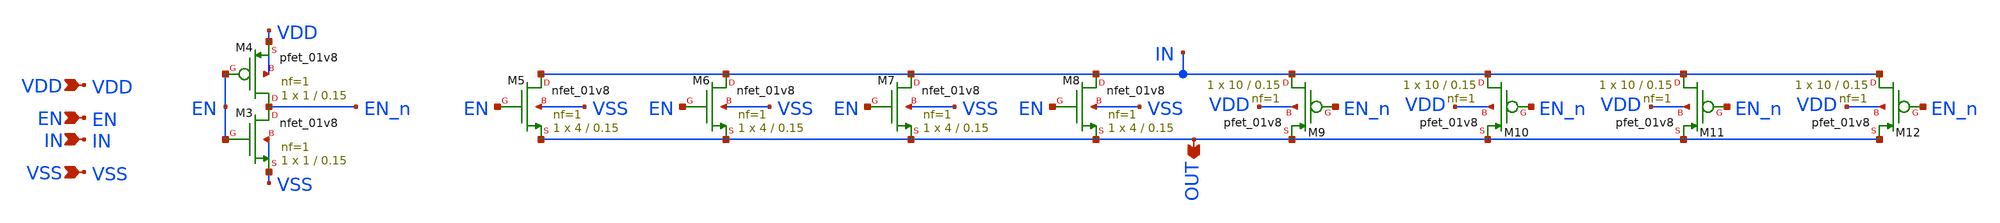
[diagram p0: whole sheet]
** sch_path: xschem/anl_switch.sch
**.subckt anl_switch IN VDD VSS EN OUT
*.ipin IN
*.ipin VDD
*.ipin VSS
*.ipin EN
*.opin OUT
XM3 EN_n EN VSS VSS sky130_fd_pr__nfet_01v8 L=0.15 W=1 nf=1 ad='int((nf+1)/2) * W/nf * 0.29' as='int((nf+2)/2) * W/nf * 0.29'
+ pd='2*int((nf+1)/2) * (W/nf + 0.29)' ps='2*int((nf+2)/2) * (W/nf + 0.29)' nrd='0.29 / W' nrs='0.29 / W'
+ sa=0 sb=0 sd=0 mult=1 m=1
XM4 EN_n EN VDD VDD sky130_fd_pr__pfet_01v8 L=0.15 W=1 nf=1 ad='int((nf+1)/2) * W/nf * 0.29' as='int((nf+2)/2) * W/nf * 0.29'
+ pd='2*int((nf+1)/2) * (W/nf + 0.29)' ps='2*int((nf+2)/2) * (W/nf + 0.29)' nrd='0.29 / W' nrs='0.29 / W'
+ sa=0 sb=0 sd=0 mult=1 m=1
XM5 IN EN OUT VSS sky130_fd_pr__nfet_01v8 L=0.15 W=4 nf=1 ad='int((nf+1)/2) * W/nf * 0.29' as='int((nf+2)/2) * W/nf * 0.29'
+ pd='2*int((nf+1)/2) * (W/nf + 0.29)' ps='2*int((nf+2)/2) * (W/nf + 0.29)' nrd='0.29 / W' nrs='0.29 / W'
+ sa=0 sb=0 sd=0 mult=1 m=1
XM6 IN EN OUT VSS sky130_fd_pr__nfet_01v8 L=0.15 W=4 nf=1 ad='int((nf+1)/2) * W/nf * 0.29' as='int((nf+2)/2) * W/nf * 0.29'
+ pd='2*int((nf+1)/2) * (W/nf + 0.29)' ps='2*int((nf+2)/2) * (W/nf + 0.29)' nrd='0.29 / W' nrs='0.29 / W'
+ sa=0 sb=0 sd=0 mult=1 m=1
XM7 IN EN OUT VSS sky130_fd_pr__nfet_01v8 L=0.15 W=4 nf=1 ad='int((nf+1)/2) * W/nf * 0.29' as='int((nf+2)/2) * W/nf * 0.29'
+ pd='2*int((nf+1)/2) * (W/nf + 0.29)' ps='2*int((nf+2)/2) * (W/nf + 0.29)' nrd='0.29 / W' nrs='0.29 / W'
+ sa=0 sb=0 sd=0 mult=1 m=1
XM8 IN EN OUT VSS sky130_fd_pr__nfet_01v8 L=0.15 W=4 nf=1 ad='int((nf+1)/2) * W/nf * 0.29' as='int((nf+2)/2) * W/nf * 0.29'
+ pd='2*int((nf+1)/2) * (W/nf + 0.29)' ps='2*int((nf+2)/2) * (W/nf + 0.29)' nrd='0.29 / W' nrs='0.29 / W'
+ sa=0 sb=0 sd=0 mult=1 m=1
XM9 IN EN_n OUT VDD sky130_fd_pr__pfet_01v8 L=0.15 W=10 nf=1 ad='int((nf+1)/2) * W/nf * 0.29' as='int((nf+2)/2) * W/nf * 0.29'
+ pd='2*int((nf+1)/2) * (W/nf + 0.29)' ps='2*int((nf+2)/2) * (W/nf + 0.29)' nrd='0.29 / W' nrs='0.29 / W'
+ sa=0 sb=0 sd=0 mult=1 m=1
XM10 IN EN_n OUT VDD sky130_fd_pr__pfet_01v8 L=0.15 W=10 nf=1 ad='int((nf+1)/2) * W/nf * 0.29' as='int((nf+2)/2) * W/nf * 0.29'
+ pd='2*int((nf+1)/2) * (W/nf + 0.29)' ps='2*int((nf+2)/2) * (W/nf + 0.29)' nrd='0.29 / W' nrs='0.29 / W'
+ sa=0 sb=0 sd=0 mult=1 m=1
XM11 IN EN_n OUT VDD sky130_fd_pr__pfet_01v8 L=0.15 W=10 nf=1 ad='int((nf+1)/2) * W/nf * 0.29' as='int((nf+2)/2) * W/nf * 0.29'
+ pd='2*int((nf+1)/2) * (W/nf + 0.29)' ps='2*int((nf+2)/2) * (W/nf + 0.29)' nrd='0.29 / W' nrs='0.29 / W'
+ sa=0 sb=0 sd=0 mult=1 m=1
XM12 IN EN_n OUT VDD sky130_fd_pr__pfet_01v8 L=0.15 W=10 nf=1 ad='int((nf+1)/2) * W/nf * 0.29' as='int((nf+2)/2) * W/nf * 0.29'
+ pd='2*int((nf+1)/2) * (W/nf + 0.29)' ps='2*int((nf+2)/2) * (W/nf + 0.29)' nrd='0.29 / W' nrs='0.29 / W'
+ sa=0 sb=0 sd=0 mult=1 m=1
**.ends
.end
